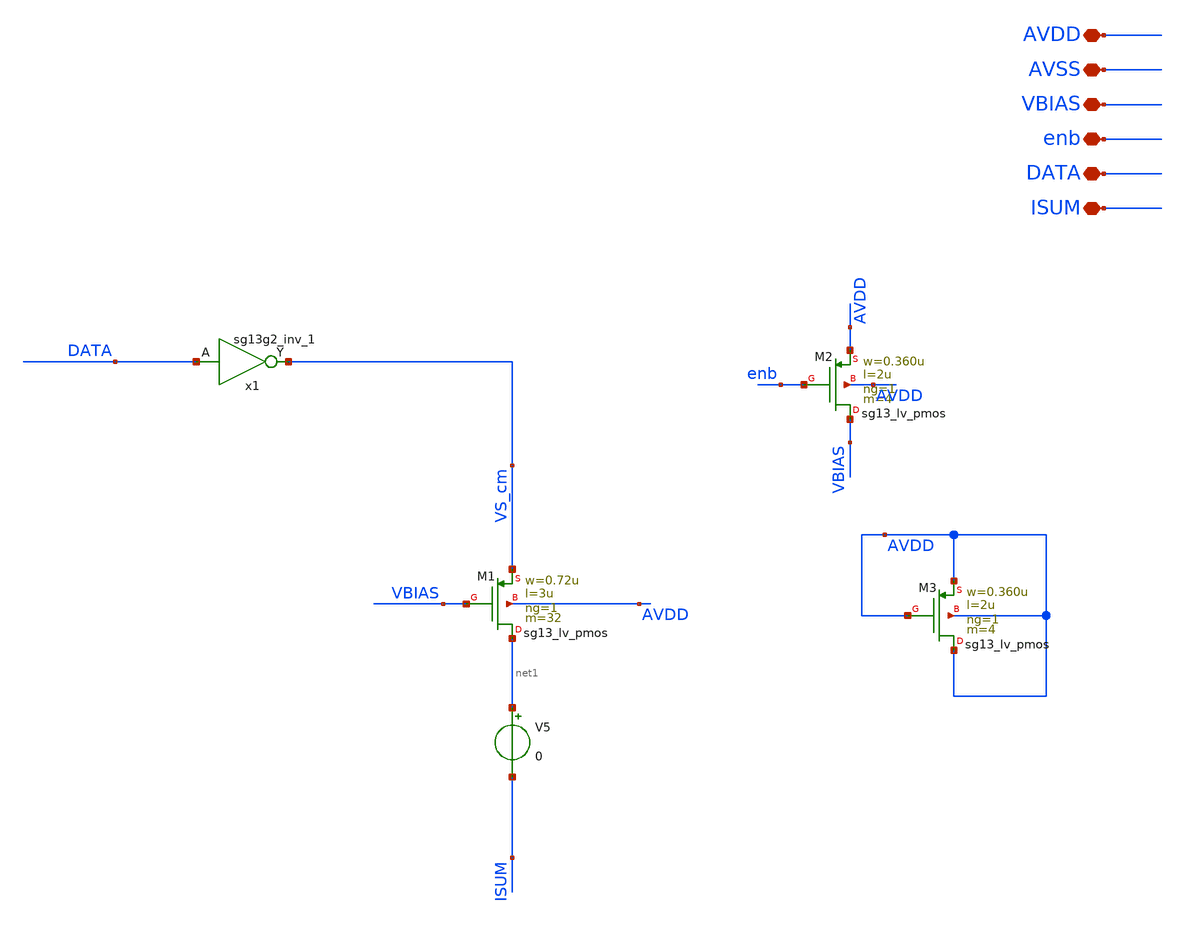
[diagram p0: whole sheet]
** sch_path: current_generator/analog/DAC/dac_thermo.sch
**.subckt dac_thermo AVDD AVSS VBIAS enb DATA ISUM
*.iopin AVDD
*.iopin AVSS
*.iopin VBIAS
*.iopin enb
*.iopin DATA
*.iopin ISUM
XM1 net1 VBIAS VS_cm AVDD sg13_lv_pmos w=0.72u l=3u ng=1 m=32 mm_ok=1
XM2 VBIAS enb AVDD AVDD sg13_lv_pmos w=0.360u l=2u ng=1 m=4 mm_ok=1
XM3 AVDD AVDD AVDD AVDD sg13_lv_pmos w=0.360u l=2u ng=1 m=4 mm_ok=1
x1 VS_cm DATA AVDD AVSS sg13g2_inv_1
V5 net1 ISUM 0
**.ends

* expanding   symbol:  sg13g2_stdcells/sg13g2_inv_1.sym # of pins=2
** sym_path: sg13g2_stdcells/sg13g2_inv_1.sym
** sch_path: sg13g2_stdcells/sg13g2_inv_1.sch
.subckt sg13g2_inv_1 Y A VDD VSS
*.opin Y
*.ipin A
*.iopin VDD
*.iopin VSS
XM1 Y A VSS VSS sg13_lv_nmos w=740.00n l=130.00n ng=1 m=1 mm_ok=1
XM2 Y A VDD VDD sg13_lv_pmos w=1.12u l=130.00n ng=1 m=1 mm_ok=1
.ends

.end
